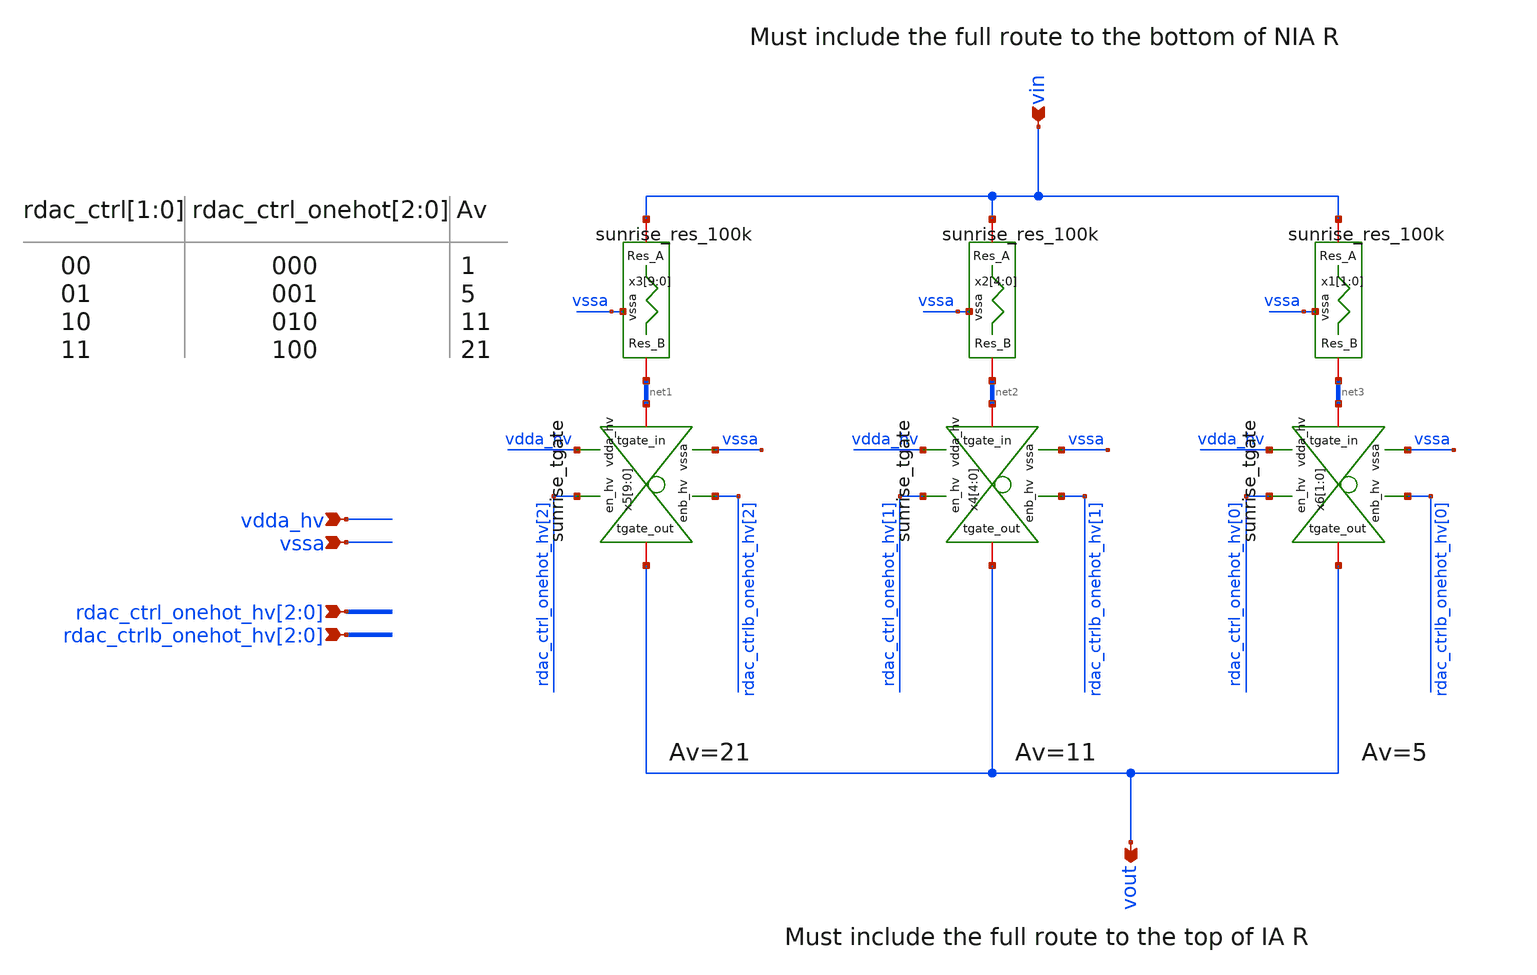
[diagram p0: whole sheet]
** sch_path: Schematics_Layout/sunrise_rdac/sunrise_rdac.sch
**.subckt sunrise_rdac vin vout rdac_ctrl_onehot_hv[2],rdac_ctrl_onehot_hv[1],rdac_ctrl_onehot_hv[0]
*+ rdac_ctrlb_onehot_hv[2],rdac_ctrlb_onehot_hv[1],rdac_ctrlb_onehot_hv[0] vdda_hv vssa
*.ipin vin
*.opin vout
*.ipin rdac_ctrl_onehot_hv[2],rdac_ctrl_onehot_hv[1],rdac_ctrl_onehot_hv[0]
*.ipin rdac_ctrlb_onehot_hv[2],rdac_ctrlb_onehot_hv[1],rdac_ctrlb_onehot_hv[0]
*.ipin vdda_hv
*.ipin vssa
x3[9] vssa net1[9] vin sunrise_res_100k
x3[8] vssa net1[8] vin sunrise_res_100k
x3[7] vssa net1[7] vin sunrise_res_100k
x3[6] vssa net1[6] vin sunrise_res_100k
x3[5] vssa net1[5] vin sunrise_res_100k
x3[4] vssa net1[4] vin sunrise_res_100k
x3[3] vssa net1[3] vin sunrise_res_100k
x3[2] vssa net1[2] vin sunrise_res_100k
x3[1] vssa net1[1] vin sunrise_res_100k
x3[0] vssa net1[0] vin sunrise_res_100k
x5[9] vdda_hv vssa rdac_ctrl_onehot_hv[2] net1[9] vout rdac_ctrlb_onehot_hv[2] sunrise_tgate
x5[8] vdda_hv vssa rdac_ctrl_onehot_hv[2] net1[8] vout rdac_ctrlb_onehot_hv[2] sunrise_tgate
x5[7] vdda_hv vssa rdac_ctrl_onehot_hv[2] net1[7] vout rdac_ctrlb_onehot_hv[2] sunrise_tgate
x5[6] vdda_hv vssa rdac_ctrl_onehot_hv[2] net1[6] vout rdac_ctrlb_onehot_hv[2] sunrise_tgate
x5[5] vdda_hv vssa rdac_ctrl_onehot_hv[2] net1[5] vout rdac_ctrlb_onehot_hv[2] sunrise_tgate
x5[4] vdda_hv vssa rdac_ctrl_onehot_hv[2] net1[4] vout rdac_ctrlb_onehot_hv[2] sunrise_tgate
x5[3] vdda_hv vssa rdac_ctrl_onehot_hv[2] net1[3] vout rdac_ctrlb_onehot_hv[2] sunrise_tgate
x5[2] vdda_hv vssa rdac_ctrl_onehot_hv[2] net1[2] vout rdac_ctrlb_onehot_hv[2] sunrise_tgate
x5[1] vdda_hv vssa rdac_ctrl_onehot_hv[2] net1[1] vout rdac_ctrlb_onehot_hv[2] sunrise_tgate
x5[0] vdda_hv vssa rdac_ctrl_onehot_hv[2] net1[0] vout rdac_ctrlb_onehot_hv[2] sunrise_tgate
x2[4] vssa net2[4] vin sunrise_res_100k
x2[3] vssa net2[3] vin sunrise_res_100k
x2[2] vssa net2[2] vin sunrise_res_100k
x2[1] vssa net2[1] vin sunrise_res_100k
x2[0] vssa net2[0] vin sunrise_res_100k
x1[1] vssa net3[1] vin sunrise_res_100k
x1[0] vssa net3[0] vin sunrise_res_100k
x4[4] vdda_hv vssa rdac_ctrl_onehot_hv[1] net2[4] vout rdac_ctrlb_onehot_hv[1] sunrise_tgate
x4[3] vdda_hv vssa rdac_ctrl_onehot_hv[1] net2[3] vout rdac_ctrlb_onehot_hv[1] sunrise_tgate
x4[2] vdda_hv vssa rdac_ctrl_onehot_hv[1] net2[2] vout rdac_ctrlb_onehot_hv[1] sunrise_tgate
x4[1] vdda_hv vssa rdac_ctrl_onehot_hv[1] net2[1] vout rdac_ctrlb_onehot_hv[1] sunrise_tgate
x4[0] vdda_hv vssa rdac_ctrl_onehot_hv[1] net2[0] vout rdac_ctrlb_onehot_hv[1] sunrise_tgate
x6[1] vdda_hv vssa rdac_ctrl_onehot_hv[0] net3[1] vout rdac_ctrlb_onehot_hv[0] sunrise_tgate
x6[0] vdda_hv vssa rdac_ctrl_onehot_hv[0] net3[0] vout rdac_ctrlb_onehot_hv[0] sunrise_tgate
**.ends
.end
